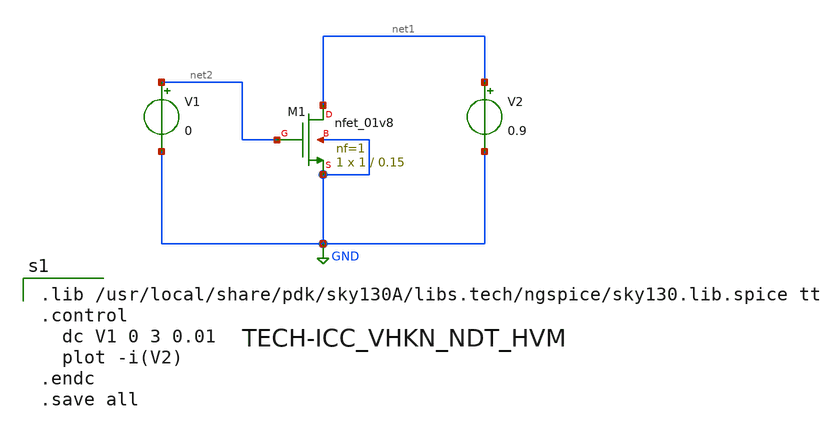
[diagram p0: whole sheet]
** sch_path: NMOS/NMOS.sch
**.subckt NMOS
XM1 net1 net2 GND GND sky130_fd_pr__nfet_01v8 L=0.15 W=1 nf=1 ad='int((1 + 1)/2) * 1 / 1 * 0.29' as='int((1 + 2)/2) * 1 / 1 * 0.29'
+ pd='2*int((1 + 1)/2) * (1 / 1 + 0.29)' ps='2*int((1 + 2)/2) * (1 / 1 + 0.29)' nrd='0.29 / 1 ' nrs='0.29 / 1 '
+ sa=0 sb=0 sd=0 mult=1 m=1
V1 net2 GND 0
V2 net1 GND 0.9
**** begin user architecture code

.lib /usr/local/share/pdk/sky130A/libs.tech/ngspice/sky130.lib.spice tt
.control
  dc V1 0 3 0.01
  plot -i(V2)
.endc
.save all


**** end user architecture code
**.ends
.GLOBAL GND
.end
